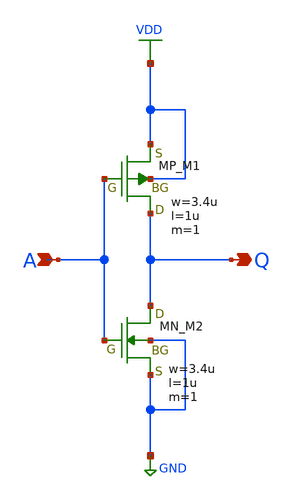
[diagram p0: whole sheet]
** sch_path: inverter/kato/inverter_kato.sch
**.subckt inverter_kato A Q
*.ipin A
*.opin Q
XM1 Q A VDD VDD PMOS w=3.4u l=1u nrd=0 nrs=0 m=1
XM2 Q A GND GND NMOS w=3.4u l=1u nrd=0 nrs=0 m=1
**.ends
.GLOBAL VDD
.GLOBAL GND
.end
